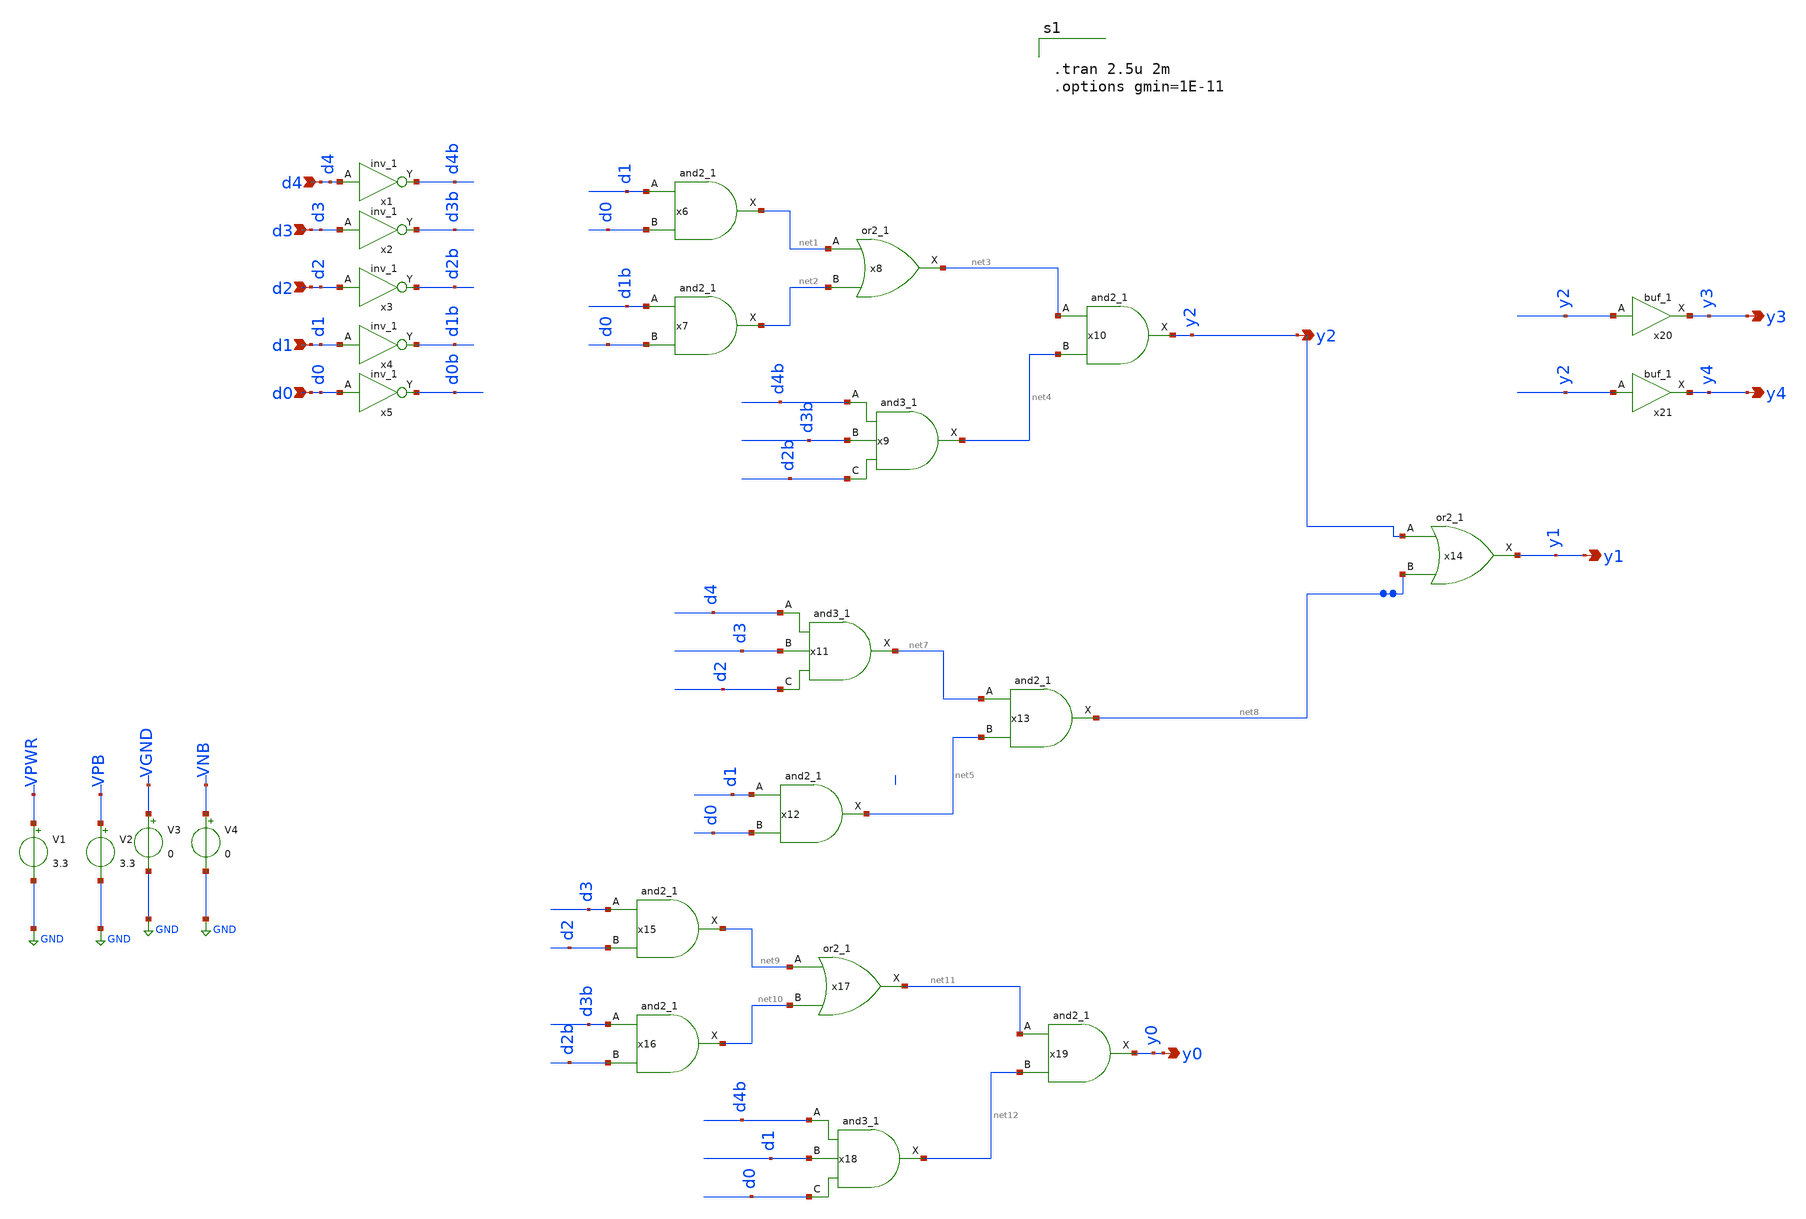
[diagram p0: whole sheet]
** sch_path: xschem/FDC/encoder1.sch
**.subckt encoder1 d4 d3 d2 d1 d0 y2 y1 y0 y3 y4
*.ipin d4
*.ipin d3
*.ipin d2
*.ipin d1
*.ipin d0
*.opin y2
*.opin y1
*.opin y0
*.opin y3
*.opin y4
x1 d4 VGND VNB VPB VPWR d4b sky130_fd_sc_hvl__inv_1
x2 d3 VGND VNB VPB VPWR d3b sky130_fd_sc_hvl__inv_1
x3 d2 VGND VNB VPB VPWR d2b sky130_fd_sc_hvl__inv_1
x4 d1 VGND VNB VPB VPWR d1b sky130_fd_sc_hvl__inv_1
x5 d0 VGND VNB VPB VPWR d0b sky130_fd_sc_hvl__inv_1
x6 d1 d0 VGND VNB VPB VPWR net1 sky130_fd_sc_hvl__and2_1
x7 d1b d0 VGND VNB VPB VPWR net2 sky130_fd_sc_hvl__and2_1
x8 net1 net2 VGND VNB VPB VPWR net3 sky130_fd_sc_hvl__or2_1
x9 d4b d3b d2b VGND VNB VPB VPWR net4 sky130_fd_sc_hvl__and3_1
x10 net3 net4 VGND VNB VPB VPWR y2 sky130_fd_sc_hvl__and2_1
x11 d4 d3 d2 VGND VNB VPB VPWR net7 sky130_fd_sc_hvl__and3_1
x12 d1 d0 VGND VNB VPB VPWR net5 sky130_fd_sc_hvl__and2_1
x13 net7 net5 VGND VNB VPB VPWR net8 sky130_fd_sc_hvl__and2_1
x14 y2 net8 VGND VNB VPB VPWR y1 sky130_fd_sc_hvl__or2_1
x15 d3 d2 VGND VNB VPB VPWR net9 sky130_fd_sc_hvl__and2_1
x16 d3b d2b VGND VNB VPB VPWR net10 sky130_fd_sc_hvl__and2_1
x17 net9 net10 VGND VNB VPB VPWR net11 sky130_fd_sc_hvl__or2_1
x18 d4b d1 d0 VGND VNB VPB VPWR net12 sky130_fd_sc_hvl__and3_1
x19 net11 net12 VGND VNB VPB VPWR y0 sky130_fd_sc_hvl__and2_1
x20 y2 VGND VNB VPB VPWR y3 sky130_fd_sc_hvl__buf_1
x21 y2 VGND VNB VPB VPWR y4 sky130_fd_sc_hvl__buf_1
V1 VPWR GND 3.3
V2 VPB GND 3.3
V3 VGND GND 0
V4 VNB GND 0
**** begin user architecture code

.lib ~/open_pdks/sky130/sky130A/libs.tech/ngspice/sky130.lib.spice tt
.include /home/vinodhini/open_pdks/sky130/sky130A/libs.ref/sky130_fd_sc_hvl/spice/sky130_fd_sc_hvl.spice

*.MODEL swmod SW(VT=0.0 VH=0.01 RON=1 ROFF=10000000000)
.param mc_mm_switch=0
.param mc_pr_switch=0


.tran 2.5u 2m
.options gmin=1E-11

**** end user architecture code
**.ends
.GLOBAL GND
.end
